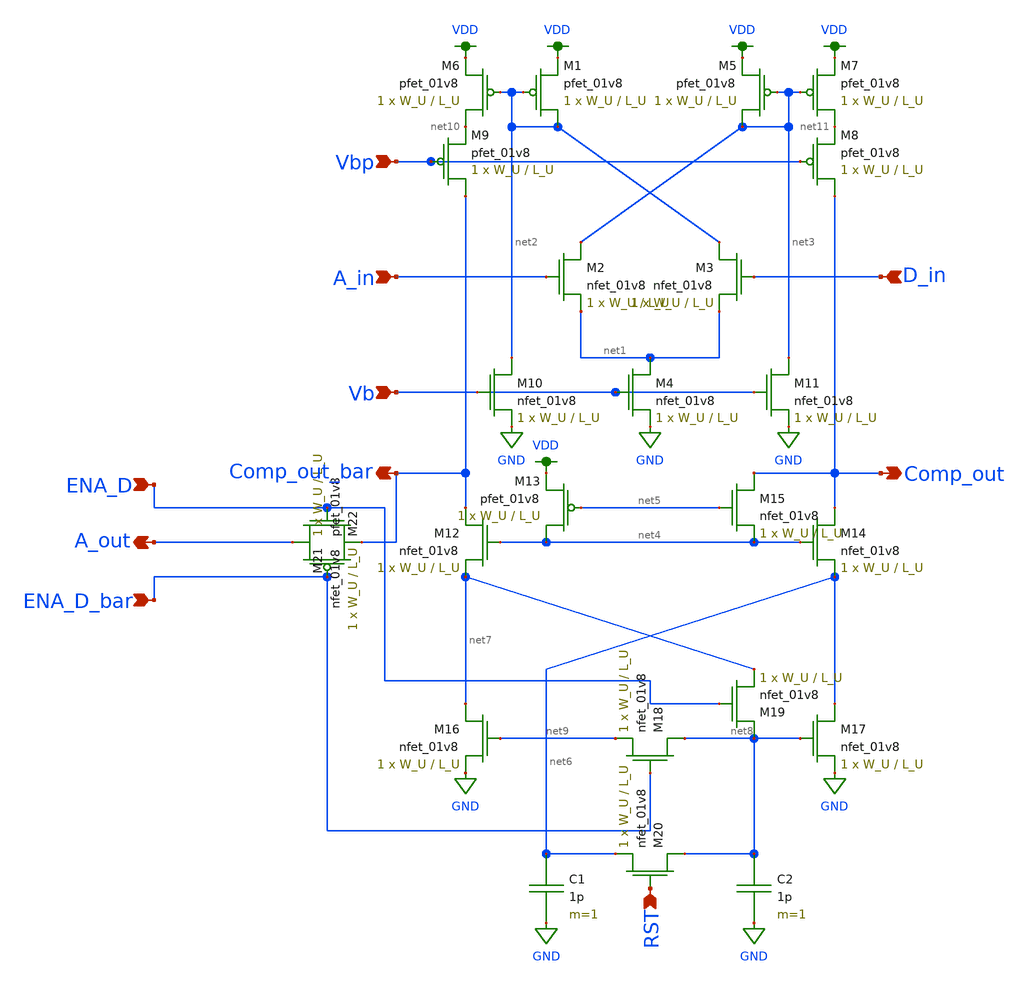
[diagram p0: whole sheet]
** sch_path: schematics/comp.sch
**.subckt comp A_in Vbp Vb A_out Comp_out_bar Comp_out ENA_D ENA_D_bar RST D_in
*.ipin A_in
*.ipin Vbp
*.ipin Vb
*.opin A_out
*.opin Comp_out_bar
*.opin Comp_out
*.ipin ENA_D
*.ipin ENA_D_bar
*.ipin RST
*.ipin D_in
XM1 net2 net2 VDD VDD sky130_fd_pr__pfet_01v8 L=L_U W=W_U nf=1 ad='int((nf+1)/2) * W/nf * 0.29' as='int((nf+2)/2) * W/nf * 0.29'
+ pd='2*int((nf+1)/2) * (W/nf + 0.29)' ps='2*int((nf+2)/2) * (W/nf + 0.29)' nrd='0.29 / W' nrs='0.29 / W'
+ sa=0 sb=0 sd=0 mult=1 m=1
XM2 net3 A_in net1 GND sky130_fd_pr__nfet_01v8 L=L_U W=W_U nf=1 ad='int((nf+1)/2) * W/nf * 0.29' as='int((nf+2)/2) * W/nf * 0.29'
+ pd='2*int((nf+1)/2) * (W/nf + 0.29)' ps='2*int((nf+2)/2) * (W/nf + 0.29)' nrd='0.29 / W' nrs='0.29 / W'
+ sa=0 sb=0 sd=0 mult=1 m=1
XM3 net2 D_in net1 GND sky130_fd_pr__nfet_01v8 L=L_U W=W_U nf=1 ad='int((nf+1)/2) * W/nf * 0.29' as='int((nf+2)/2) * W/nf * 0.29'
+ pd='2*int((nf+1)/2) * (W/nf + 0.29)' ps='2*int((nf+2)/2) * (W/nf + 0.29)' nrd='0.29 / W' nrs='0.29 / W'
+ sa=0 sb=0 sd=0 mult=1 m=1
XM4 net1 Vb GND GND sky130_fd_pr__nfet_01v8 L=L_U W=W_U nf=1 ad='int((nf+1)/2) * W/nf * 0.29' as='int((nf+2)/2) * W/nf * 0.29'
+ pd='2*int((nf+1)/2) * (W/nf + 0.29)' ps='2*int((nf+2)/2) * (W/nf + 0.29)' nrd='0.29 / W' nrs='0.29 / W'
+ sa=0 sb=0 sd=0 mult=1 m=1
XM5 net3 net3 VDD VDD sky130_fd_pr__pfet_01v8 L=L_U W=W_U nf=1 ad='int((nf+1)/2) * W/nf * 0.29' as='int((nf+2)/2) * W/nf * 0.29'
+ pd='2*int((nf+1)/2) * (W/nf + 0.29)' ps='2*int((nf+2)/2) * (W/nf + 0.29)' nrd='0.29 / W' nrs='0.29 / W'
+ sa=0 sb=0 sd=0 mult=1 m=1
XM6 net10 net2 VDD VDD sky130_fd_pr__pfet_01v8 L=L_U W=W_U nf=1 ad='int((nf+1)/2) * W/nf * 0.29' as='int((nf+2)/2) * W/nf * 0.29'
+ pd='2*int((nf+1)/2) * (W/nf + 0.29)' ps='2*int((nf+2)/2) * (W/nf + 0.29)' nrd='0.29 / W' nrs='0.29 / W'
+ sa=0 sb=0 sd=0 mult=1 m=1
XM7 net11 net3 VDD VDD sky130_fd_pr__pfet_01v8 L=L_U W=W_U nf=1 ad='int((nf+1)/2) * W/nf * 0.29' as='int((nf+2)/2) * W/nf * 0.29'
+ pd='2*int((nf+1)/2) * (W/nf + 0.29)' ps='2*int((nf+2)/2) * (W/nf + 0.29)' nrd='0.29 / W' nrs='0.29 / W'
+ sa=0 sb=0 sd=0 mult=1 m=1
XM8 Comp_out Vbp net11 VDD sky130_fd_pr__pfet_01v8 L=L_U W=W_U nf=1 ad='int((nf+1)/2) * W/nf * 0.29'
+ as='int((nf+2)/2) * W/nf * 0.29' pd='2*int((nf+1)/2) * (W/nf + 0.29)' ps='2*int((nf+2)/2) * (W/nf + 0.29)'
+ nrd='0.29 / W' nrs='0.29 / W' sa=0 sb=0 sd=0 mult=1 m=1
XM9 Comp_out_bar Vbp net10 VDD sky130_fd_pr__pfet_01v8 L=L_U W=W_U nf=1 ad='int((nf+1)/2) * W/nf * 0.29'
+ as='int((nf+2)/2) * W/nf * 0.29' pd='2*int((nf+1)/2) * (W/nf + 0.29)' ps='2*int((nf+2)/2) * (W/nf + 0.29)'
+ nrd='0.29 / W' nrs='0.29 / W' sa=0 sb=0 sd=0 mult=1 m=1
XM10 net2 Vb GND GND sky130_fd_pr__nfet_01v8 L=L_U W=W_U nf=1 ad='int((nf+1)/2) * W/nf * 0.29' as='int((nf+2)/2) * W/nf * 0.29'
+ pd='2*int((nf+1)/2) * (W/nf + 0.29)' ps='2*int((nf+2)/2) * (W/nf + 0.29)' nrd='0.29 / W' nrs='0.29 / W'
+ sa=0 sb=0 sd=0 mult=1 m=1
XM11 net3 Vb GND GND sky130_fd_pr__nfet_01v8 L=L_U W=W_U nf=1 ad='int((nf+1)/2) * W/nf * 0.29' as='int((nf+2)/2) * W/nf * 0.29'
+ pd='2*int((nf+1)/2) * (W/nf + 0.29)' ps='2*int((nf+2)/2) * (W/nf + 0.29)' nrd='0.29 / W' nrs='0.29 / W'
+ sa=0 sb=0 sd=0 mult=1 m=1
XM12 Comp_out_bar net4 net7 GND sky130_fd_pr__nfet_01v8 L=L_U W=W_U nf=1 ad='int((nf+1)/2) * W/nf * 0.29'
+ as='int((nf+2)/2) * W/nf * 0.29' pd='2*int((nf+1)/2) * (W/nf + 0.29)' ps='2*int((nf+2)/2) * (W/nf + 0.29)'
+ nrd='0.29 / W' nrs='0.29 / W' sa=0 sb=0 sd=0 mult=1 m=1
XM13 net4 net5 VDD VDD sky130_fd_pr__pfet_01v8 L=L_U W=W_U nf=1 ad='int((nf+1)/2) * W/nf * 0.29' as='int((nf+2)/2) * W/nf * 0.29'
+ pd='2*int((nf+1)/2) * (W/nf + 0.29)' ps='2*int((nf+2)/2) * (W/nf + 0.29)' nrd='0.29 / W' nrs='0.29 / W'
+ sa=0 sb=0 sd=0 mult=1 m=1
XM14 Comp_out net4 net6 GND sky130_fd_pr__nfet_01v8 L=L_U W=W_U nf=1 ad='int((nf+1)/2) * W/nf * 0.29'
+ as='int((nf+2)/2) * W/nf * 0.29' pd='2*int((nf+1)/2) * (W/nf + 0.29)' ps='2*int((nf+2)/2) * (W/nf + 0.29)'
+ nrd='0.29 / W' nrs='0.29 / W' sa=0 sb=0 sd=0 mult=1 m=1
XM15 Comp_out net5 net4 GND sky130_fd_pr__nfet_01v8 L=L_U W=W_U nf=1 ad='int((nf+1)/2) * W/nf * 0.29'
+ as='int((nf+2)/2) * W/nf * 0.29' pd='2*int((nf+1)/2) * (W/nf + 0.29)' ps='2*int((nf+2)/2) * (W/nf + 0.29)'
+ nrd='0.29 / W' nrs='0.29 / W' sa=0 sb=0 sd=0 mult=1 m=1
XM16 net7 net9 GND GND sky130_fd_pr__nfet_01v8 L=L_U W=W_U nf=1 ad='int((nf+1)/2) * W/nf * 0.29' as='int((nf+2)/2) * W/nf * 0.29'
+ pd='2*int((nf+1)/2) * (W/nf + 0.29)' ps='2*int((nf+2)/2) * (W/nf + 0.29)' nrd='0.29 / W' nrs='0.29 / W'
+ sa=0 sb=0 sd=0 mult=1 m=1
XM17 net6 net8 GND GND sky130_fd_pr__nfet_01v8 L=L_U W=W_U nf=1 ad='int((nf+1)/2) * W/nf * 0.29' as='int((nf+2)/2) * W/nf * 0.29'
+ pd='2*int((nf+1)/2) * (W/nf + 0.29)' ps='2*int((nf+2)/2) * (W/nf + 0.29)' nrd='0.29 / W' nrs='0.29 / W'
+ sa=0 sb=0 sd=0 mult=1 m=1
XM18 net8 ENA_D_bar net9 GND sky130_fd_pr__nfet_01v8 L=L_U W=W_U nf=1 ad='int((nf+1)/2) * W/nf * 0.29'
+ as='int((nf+2)/2) * W/nf * 0.29' pd='2*int((nf+1)/2) * (W/nf + 0.29)' ps='2*int((nf+2)/2) * (W/nf + 0.29)'
+ nrd='0.29 / W' nrs='0.29 / W' sa=0 sb=0 sd=0 mult=1 m=1
XM19 net8 ENA_D net7 GND sky130_fd_pr__nfet_01v8 L=L_U W=W_U nf=1 ad='int((nf+1)/2) * W/nf * 0.29' as='int((nf+2)/2) * W/nf * 0.29'
+ pd='2*int((nf+1)/2) * (W/nf + 0.29)' ps='2*int((nf+2)/2) * (W/nf + 0.29)' nrd='0.29 / W' nrs='0.29 / W'
+ sa=0 sb=0 sd=0 mult=1 m=1
XM20 net8 RST net6 GND sky130_fd_pr__nfet_01v8 L=L_U W=W_U nf=1 ad='int((nf+1)/2) * W/nf * 0.29' as='int((nf+2)/2) * W/nf * 0.29'
+ pd='2*int((nf+1)/2) * (W/nf + 0.29)' ps='2*int((nf+2)/2) * (W/nf + 0.29)' nrd='0.29 / W' nrs='0.29 / W'
+ sa=0 sb=0 sd=0 mult=1 m=1
C1 net6 GND 1p m=1
C2 net8 GND 1p m=1
XM21 A_out ENA_D Comp_out_bar GND sky130_fd_pr__nfet_01v8 L=L_U W=W_U nf=1 ad='int((nf+1)/2) * W/nf * 0.29'
+ as='int((nf+2)/2) * W/nf * 0.29' pd='2*int((nf+1)/2) * (W/nf + 0.29)' ps='2*int((nf+2)/2) * (W/nf + 0.29)'
+ nrd='0.29 / W' nrs='0.29 / W' sa=0 sb=0 sd=0 mult=1 m=1
XM22 A_out ENA_D_bar Comp_out_bar VDD sky130_fd_pr__pfet_01v8 L=L_U W=W_U nf=1 ad='int((nf+1)/2) * W/nf * 0.29'
+ as='int((nf+2)/2) * W/nf * 0.29' pd='2*int((nf+1)/2) * (W/nf + 0.29)' ps='2*int((nf+2)/2) * (W/nf + 0.29)'
+ nrd='0.29 / W' nrs='0.29 / W' sa=0 sb=0 sd=0 mult=1 m=1
**.ends
.GLOBAL VDD
.GLOBAL GND
.end
